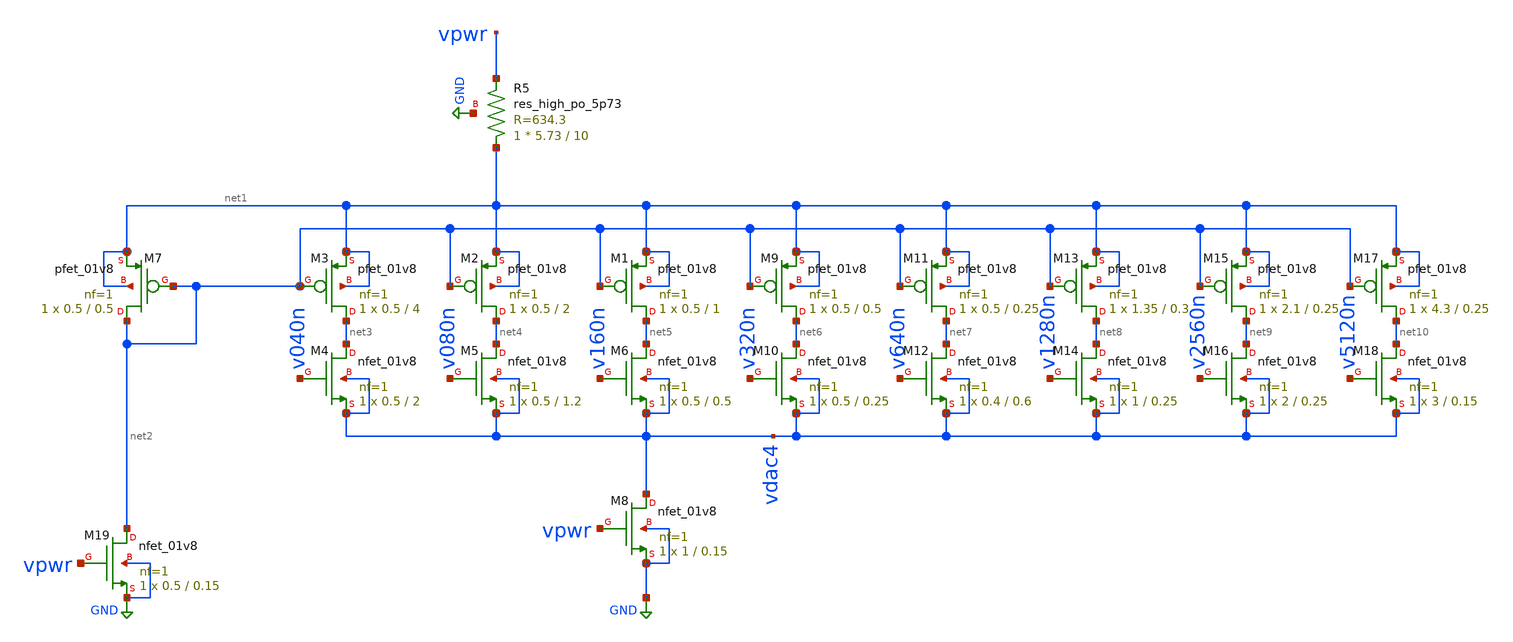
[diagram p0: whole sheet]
** sch_path: xschem/bdac.sch
**.subckt bdac
XM1 net5 net2 net1 net1 sky130_fd_pr__pfet_01v8 L=1 W=0.5 nf=1 ad='int((nf+1)/2) * W/nf * 0.29' as='int((nf+2)/2) * W/nf * 0.29'
+ pd='2*int((nf+1)/2) * (W/nf + 0.29)' ps='2*int((nf+2)/2) * (W/nf + 0.29)' nrd='0.29 / W' nrs='0.29 / W'
+ sa=0 sb=0 sd=0 mult=1 m=1
XM2 net4 net2 net1 net1 sky130_fd_pr__pfet_01v8 L=2 W=0.5 nf=1 ad='int((nf+1)/2) * W/nf * 0.29' as='int((nf+2)/2) * W/nf * 0.29'
+ pd='2*int((nf+1)/2) * (W/nf + 0.29)' ps='2*int((nf+2)/2) * (W/nf + 0.29)' nrd='0.29 / W' nrs='0.29 / W'
+ sa=0 sb=0 sd=0 mult=1 m=1
XM3 net3 net2 net1 net1 sky130_fd_pr__pfet_01v8 L=4 W=0.5 nf=1 ad='int((nf+1)/2) * W/nf * 0.29' as='int((nf+2)/2) * W/nf * 0.29'
+ pd='2*int((nf+1)/2) * (W/nf + 0.29)' ps='2*int((nf+2)/2) * (W/nf + 0.29)' nrd='0.29 / W' nrs='0.29 / W'
+ sa=0 sb=0 sd=0 mult=1 m=1
XM7 net2 net2 net1 net1 sky130_fd_pr__pfet_01v8 L=0.5 W=0.5 nf=1 ad='int((nf+1)/2) * W/nf * 0.29' as='int((nf+2)/2) * W/nf * 0.29'
+ pd='2*int((nf+1)/2) * (W/nf + 0.29)' ps='2*int((nf+2)/2) * (W/nf + 0.29)' nrd='0.29 / W' nrs='0.29 / W'
+ sa=0 sb=0 sd=0 mult=1 m=1
XM4 net3 v040n vdac4 vdac4 sky130_fd_pr__nfet_01v8 L=2 W=0.5 nf=1 ad='int((nf+1)/2) * W/nf * 0.29' as='int((nf+2)/2) * W/nf * 0.29'
+ pd='2*int((nf+1)/2) * (W/nf + 0.29)' ps='2*int((nf+2)/2) * (W/nf + 0.29)' nrd='0.29 / W' nrs='0.29 / W'
+ sa=0 sb=0 sd=0 mult=1 m=1
XM5 net4 v080n vdac4 vdac4 sky130_fd_pr__nfet_01v8 L=1.2 W=0.5 nf=1 ad='int((nf+1)/2) * W/nf * 0.29'
+ as='int((nf+2)/2) * W/nf * 0.29' pd='2*int((nf+1)/2) * (W/nf + 0.29)' ps='2*int((nf+2)/2) * (W/nf + 0.29)'
+ nrd='0.29 / W' nrs='0.29 / W' sa=0 sb=0 sd=0 mult=1 m=1
XM6 net5 v160n vdac4 vdac4 sky130_fd_pr__nfet_01v8 L=0.5 W=0.5 nf=1 ad='int((nf+1)/2) * W/nf * 0.29'
+ as='int((nf+2)/2) * W/nf * 0.29' pd='2*int((nf+1)/2) * (W/nf + 0.29)' ps='2*int((nf+2)/2) * (W/nf + 0.29)'
+ nrd='0.29 / W' nrs='0.29 / W' sa=0 sb=0 sd=0 mult=1 m=1
XM8 vdac4 vpwr GND GND sky130_fd_pr__nfet_01v8 L=0.15 W=1 nf=1 ad='int((nf+1)/2) * W/nf * 0.29' as='int((nf+2)/2) * W/nf * 0.29'
+ pd='2*int((nf+1)/2) * (W/nf + 0.29)' ps='2*int((nf+2)/2) * (W/nf + 0.29)' nrd='0.29 / W' nrs='0.29 / W'
+ sa=0 sb=0 sd=0 mult=1 m=1
XM9 net6 net2 net1 net1 sky130_fd_pr__pfet_01v8 L=0.5 W=0.5 nf=1 ad='int((nf+1)/2) * W/nf * 0.29' as='int((nf+2)/2) * W/nf * 0.29'
+ pd='2*int((nf+1)/2) * (W/nf + 0.29)' ps='2*int((nf+2)/2) * (W/nf + 0.29)' nrd='0.29 / W' nrs='0.29 / W'
+ sa=0 sb=0 sd=0 mult=1 m=1
XM10 net6 v320n vdac4 vdac4 sky130_fd_pr__nfet_01v8 L=0.25 W=0.5 nf=1 ad='int((nf+1)/2) * W/nf * 0.29'
+ as='int((nf+2)/2) * W/nf * 0.29' pd='2*int((nf+1)/2) * (W/nf + 0.29)' ps='2*int((nf+2)/2) * (W/nf + 0.29)'
+ nrd='0.29 / W' nrs='0.29 / W' sa=0 sb=0 sd=0 mult=1 m=1
XM11 net7 net2 net1 net1 sky130_fd_pr__pfet_01v8 L=0.25 W=0.5 nf=1 ad='int((nf+1)/2) * W/nf * 0.29' as='int((nf+2)/2) * W/nf * 0.29'
+ pd='2*int((nf+1)/2) * (W/nf + 0.29)' ps='2*int((nf+2)/2) * (W/nf + 0.29)' nrd='0.29 / W' nrs='0.29 / W'
+ sa=0 sb=0 sd=0 mult=1 m=1
XM12 net7 v640n vdac4 vdac4 sky130_fd_pr__nfet_01v8 L=0.6 W=0.4 nf=1 ad='int((nf+1)/2) * W/nf * 0.29'
+ as='int((nf+2)/2) * W/nf * 0.29' pd='2*int((nf+1)/2) * (W/nf + 0.29)' ps='2*int((nf+2)/2) * (W/nf + 0.29)'
+ nrd='0.29 / W' nrs='0.29 / W' sa=0 sb=0 sd=0 mult=1 m=1
XM13 net8 net2 net1 net1 sky130_fd_pr__pfet_01v8 L=0.3 W=1.35 nf=1 ad='int((nf+1)/2) * W/nf * 0.29' as='int((nf+2)/2) * W/nf * 0.29'
+ pd='2*int((nf+1)/2) * (W/nf + 0.29)' ps='2*int((nf+2)/2) * (W/nf + 0.29)' nrd='0.29 / W' nrs='0.29 / W'
+ sa=0 sb=0 sd=0 mult=1 m=1
XM14 net8 v1280n vdac4 vdac4 sky130_fd_pr__nfet_01v8 L=0.25 W=1 nf=1 ad='int((nf+1)/2) * W/nf * 0.29'
+ as='int((nf+2)/2) * W/nf * 0.29' pd='2*int((nf+1)/2) * (W/nf + 0.29)' ps='2*int((nf+2)/2) * (W/nf + 0.29)'
+ nrd='0.29 / W' nrs='0.29 / W' sa=0 sb=0 sd=0 mult=1 m=1
XM15 net9 net2 net1 net1 sky130_fd_pr__pfet_01v8 L=0.25 W=2.1 nf=1 ad='int((nf+1)/2) * W/nf * 0.29' as='int((nf+2)/2) * W/nf * 0.29'
+ pd='2*int((nf+1)/2) * (W/nf + 0.29)' ps='2*int((nf+2)/2) * (W/nf + 0.29)' nrd='0.29 / W' nrs='0.29 / W'
+ sa=0 sb=0 sd=0 mult=1 m=1
XM16 net9 v2560n vdac4 vdac4 sky130_fd_pr__nfet_01v8 L=0.25 W=2 nf=1 ad='int((nf+1)/2) * W/nf * 0.29'
+ as='int((nf+2)/2) * W/nf * 0.29' pd='2*int((nf+1)/2) * (W/nf + 0.29)' ps='2*int((nf+2)/2) * (W/nf + 0.29)'
+ nrd='0.29 / W' nrs='0.29 / W' sa=0 sb=0 sd=0 mult=1 m=1
XM17 net10 net2 net1 net1 sky130_fd_pr__pfet_01v8 L=0.25 W=4.3 nf=1 ad='int((nf+1)/2) * W/nf * 0.29'
+ as='int((nf+2)/2) * W/nf * 0.29' pd='2*int((nf+1)/2) * (W/nf + 0.29)' ps='2*int((nf+2)/2) * (W/nf + 0.29)'
+ nrd='0.29 / W' nrs='0.29 / W' sa=0 sb=0 sd=0 mult=1 m=1
XM18 net10 v5120n vdac4 vdac4 sky130_fd_pr__nfet_01v8 L=0.15 W=3 nf=1 ad='int((nf+1)/2) * W/nf * 0.29'
+ as='int((nf+2)/2) * W/nf * 0.29' pd='2*int((nf+1)/2) * (W/nf + 0.29)' ps='2*int((nf+2)/2) * (W/nf + 0.29)'
+ nrd='0.29 / W' nrs='0.29 / W' sa=0 sb=0 sd=0 mult=1 m=1
XM19 net2 vpwr GND GND sky130_fd_pr__nfet_01v8 L=0.15 W=0.5 nf=1 ad='int((nf+1)/2) * W/nf * 0.29' as='int((nf+2)/2) * W/nf * 0.29'
+ pd='2*int((nf+1)/2) * (W/nf + 0.29)' ps='2*int((nf+2)/2) * (W/nf + 0.29)' nrd='0.29 / W' nrs='0.29 / W'
+ sa=0 sb=0 sd=0 mult=1 m=1
XR5 net1 vpwr GND sky130_fd_pr__res_high_po_5p73 L=10 mult=1 m=1
**.ends
.GLOBAL GND
.end
